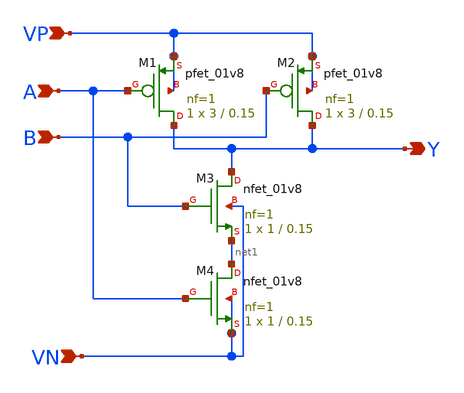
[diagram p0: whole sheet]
** sch_path: APIC-UTS/schematic/goldwin_nand_v2/goldwin_nand_v2.sch
**.subckt goldwin_nand_v2 A B VP VN Y
*.ipin A
*.ipin B
*.ipin VP
*.ipin VN
*.opin Y
XM1 Y A VP VP sky130_fd_pr__pfet_01v8 L=0.15 W=3 nf=1 ad='int((nf+1)/2) * W/nf * 0.29' as='int((nf+2)/2) * W/nf * 0.29'
+ pd='2*int((nf+1)/2) * (W/nf + 0.29)' ps='2*int((nf+2)/2) * (W/nf + 0.29)' nrd='0.29 / W' nrs='0.29 / W'
+ sa=0 sb=0 sd=0 mult=1 m=1
XM2 Y B VP VP sky130_fd_pr__pfet_01v8 L=0.15 W=3 nf=1 ad='int((nf+1)/2) * W/nf * 0.29' as='int((nf+2)/2) * W/nf * 0.29'
+ pd='2*int((nf+1)/2) * (W/nf + 0.29)' ps='2*int((nf+2)/2) * (W/nf + 0.29)' nrd='0.29 / W' nrs='0.29 / W'
+ sa=0 sb=0 sd=0 mult=1 m=1
XM3 Y B net1 VN sky130_fd_pr__nfet_01v8 L=0.15 W=1 nf=1 ad='int((nf+1)/2) * W/nf * 0.29' as='int((nf+2)/2) * W/nf * 0.29'
+ pd='2*int((nf+1)/2) * (W/nf + 0.29)' ps='2*int((nf+2)/2) * (W/nf + 0.29)' nrd='0.29 / W' nrs='0.29 / W'
+ sa=0 sb=0 sd=0 mult=1 m=1
XM4 net1 A VN VN sky130_fd_pr__nfet_01v8 L=0.15 W=1 nf=1 ad='int((nf+1)/2) * W/nf * 0.29' as='int((nf+2)/2) * W/nf * 0.29'
+ pd='2*int((nf+1)/2) * (W/nf + 0.29)' ps='2*int((nf+2)/2) * (W/nf + 0.29)' nrd='0.29 / W' nrs='0.29 / W'
+ sa=0 sb=0 sd=0 mult=1 m=1
**.ends
.end
